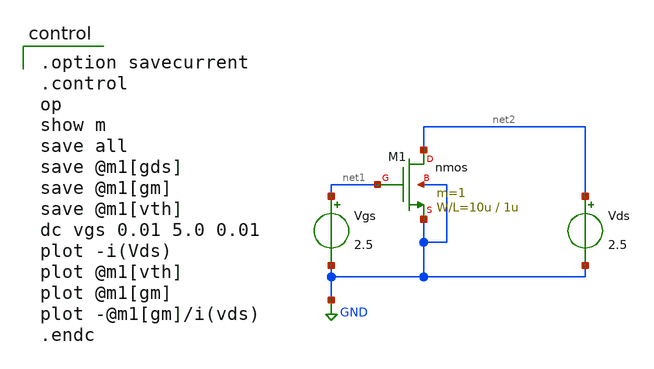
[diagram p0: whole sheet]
** sch_path: OR1/PTC06/opamp/nfet_idvgs.sch
**.subckt nfet_idvgs
Vgs net1 GND 2.5
Vds net2 GND 2.5
M1 net2 net1 GND GND nmos L=1u W=10u m=1
**** begin user architecture code

.option savecurrent
.control
op
show m
save all
save @m1[gds]
save @m1[gm]
save @m1[vth]
dc vgs 0.01 5.0 0.01
plot -i(Vds)
plot @m1[vth]
plot @m1[gm]
plot -@m1[gm]/i(vds)
.endc

 .include $::LIB/mos.lib
.include $::LIB/passive.lib
.include $::LIB/diode.lib
**** end user architecture code
**.ends
.GLOBAL GND
.end
